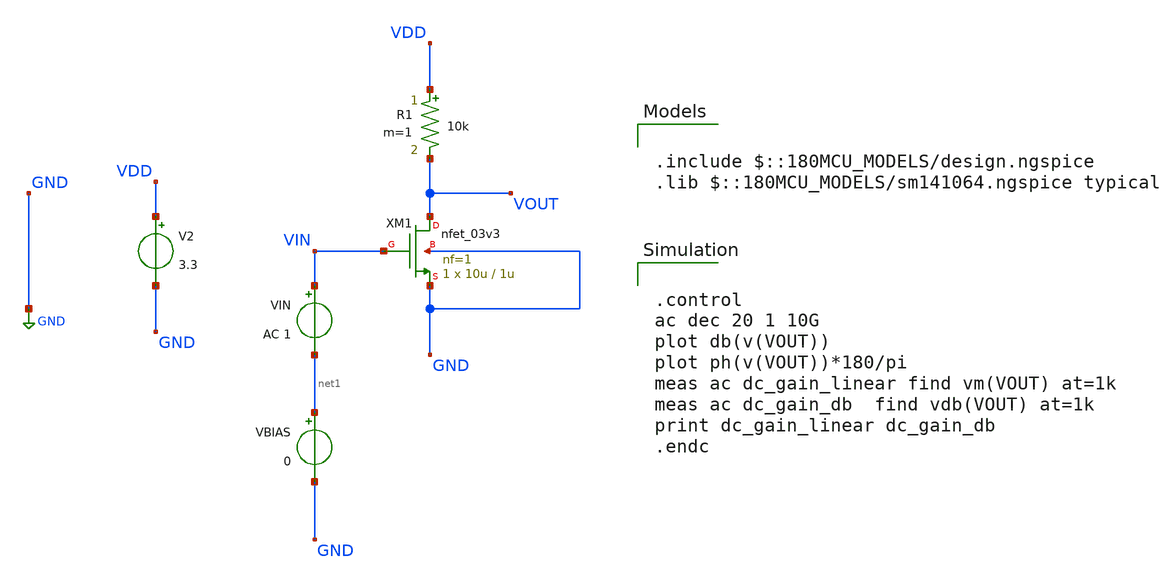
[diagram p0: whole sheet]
** sch_path: designs/sophiazhu/session_1/cs_res_load_ac.sch
**.subckt cs_res_load_ac
XM1 VOUT VIN GND GND nfet_03v3 L=1u W=10u nf=1 ad='int((nf+1)/2) * W/nf * 0.18u' as='int((nf+2)/2) * W/nf * 0.18u'
+ pd='2*int((nf+1)/2) * (W/nf + 0.18u)' ps='2*int((nf+2)/2) * (W/nf + 0.18u)' nrd='0.18u / W' nrs='0.18u / W'
+ sa=0 sb=0 sd=0 m=1
R1 VDD VOUT 10k m=1
V2 VDD GND 3.3
VBIAS net1 GND 0
VIN VIN net1 AC 1
**** begin user architecture code


.control
ac dec 20 1 10G
plot db(v(VOUT))
plot ph(v(VOUT))*180/pi
meas ac dc_gain_linear find vm(VOUT) at=1k
meas ac dc_gain_db  find vdb(VOUT) at=1k
print dc_gain_linear dc_gain_db
.endc



.include $::180MCU_MODELS/design.ngspice
.lib $::180MCU_MODELS/sm141064.ngspice typical

**** end user architecture code
**.ends
.GLOBAL GND
.end
